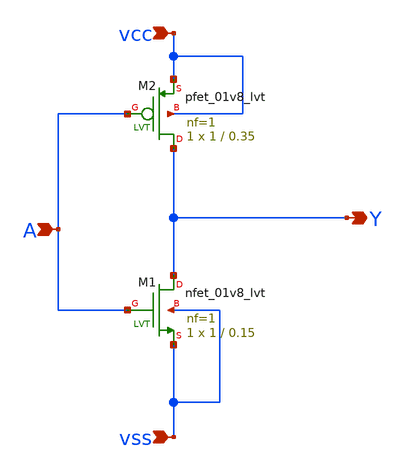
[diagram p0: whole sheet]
** sch_path: fedevel_inverter.sch
**.subckt fedevel_inverter A vss vcc Y
*.ipin A
*.ipin vss
*.ipin vcc
*.opin Y
XM1 Y A vss vss sky130_fd_pr__nfet_01v8_lvt L=0.15 W=1 nf=1 ad='int((nf+1)/2) * W/nf * 0.29' as='int((nf+2)/2) * W/nf * 0.29'
+ pd='2*int((nf+1)/2) * (W/nf + 0.29)' ps='2*int((nf+2)/2) * (W/nf + 0.29)' nrd='0.29 / W' nrs='0.29 / W'
+ sa=0 sb=0 sd=0 mult=1 m=1
XM2 Y A vcc vcc sky130_fd_pr__pfet_01v8_lvt L=0.35 W=1 nf=1 ad='int((nf+1)/2) * W/nf * 0.29' as='int((nf+2)/2) * W/nf * 0.29'
+ pd='2*int((nf+1)/2) * (W/nf + 0.29)' ps='2*int((nf+2)/2) * (W/nf + 0.29)' nrd='0.29 / W' nrs='0.29 / W'
+ sa=0 sb=0 sd=0 mult=1 m=1
**.ends
.end
